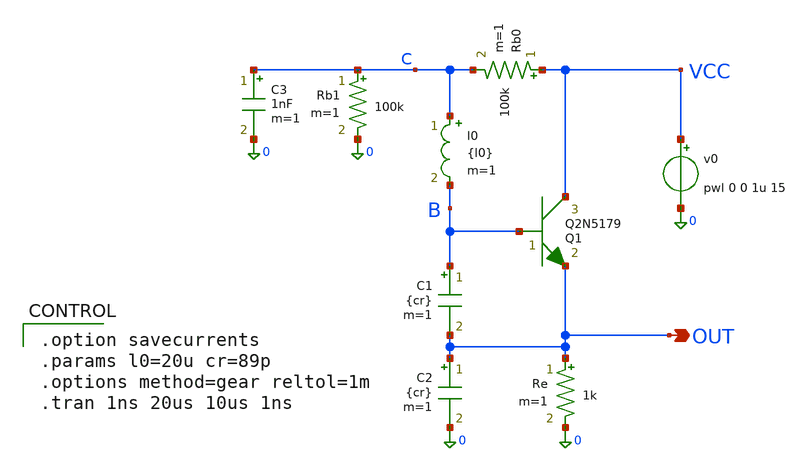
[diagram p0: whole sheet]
** sch_path: xschem_library_oa/ngspice/colpitts_xschem/schematic/colpitts_xschem.sch
* Copyright (C) 1998-2024 Stefan Frederik Schippers
* This program is free software; you can redistribute it and/or modify
* it under the terms of the GNU General Public License as published by
* the Free Software Foundation; either version 2 of the License, or
* (at your option) any later version.
* This program is distributed in the hope that it will be useful,
* but WITHOUT ANY WARRANTY; without even the implied warranty of
* MERCHANTABILITY or FITNESS FOR A PARTICULAR PURPOSE.  See the
* GNU General Public License for more details.
* You should have received a copy of the GNU General Public License
* along with this program; if not, write to the Free Software
**.subckt colpitts_xschem OUT
*.opin OUT
l0 C B {l0} m=1
C3 C 0 1nF m=1
Rb0 VCC C 100k m=1
v0 VCC 0 pwl 0 0 1u 15
Re OUT 0 1k m=1
Rb1 C 0 100k m=1
C2 OUT 0 {cr} m=1
C1 B OUT {cr} m=1
Q1 VCC B OUT Q2N5179 area=1 m=1
**** begin user architecture code

.MODEL Q2N5179  NPN (IS=1.55467e-17 BF=296.182 NF=0.850014 VAF=10 IKF=0.00544635 ISE=2.01913e-14
+ NE=1.54276 BR=19.550 NR=0.825166 VAR=73.1109 IKR=0.0544635 ISC=1e-160 NC=2.9688 RB=21.0221 IRB=0.478136
+ RBM=0.1384250 RE=0.000646335 RC=3.0552 XTB=0.582018 XTI=1 EG=1.06135 CJE=1.08982e-12 VJE=0.99 MJE=0.230
+ TF=2.15066e-11 XTF=1000 VTF=1.33967 ITF=0.0010 CJC=1.89423e-12 VJC=0.95 MJC=0.23 XCJC=0.4084790 FC=0.1 CJS=0
+ VJS=0.75 MJS=0.50 TR=1e-07 PTF=0 KF=0 AF=1)


**** end user architecture code
**.ends
**** begin user architecture code

.option savecurrents
.params l0=20u cr=89p
.options method=gear reltol=1m
.tran 1ns 20us 10us 1ns


**** end user architecture code
.end
